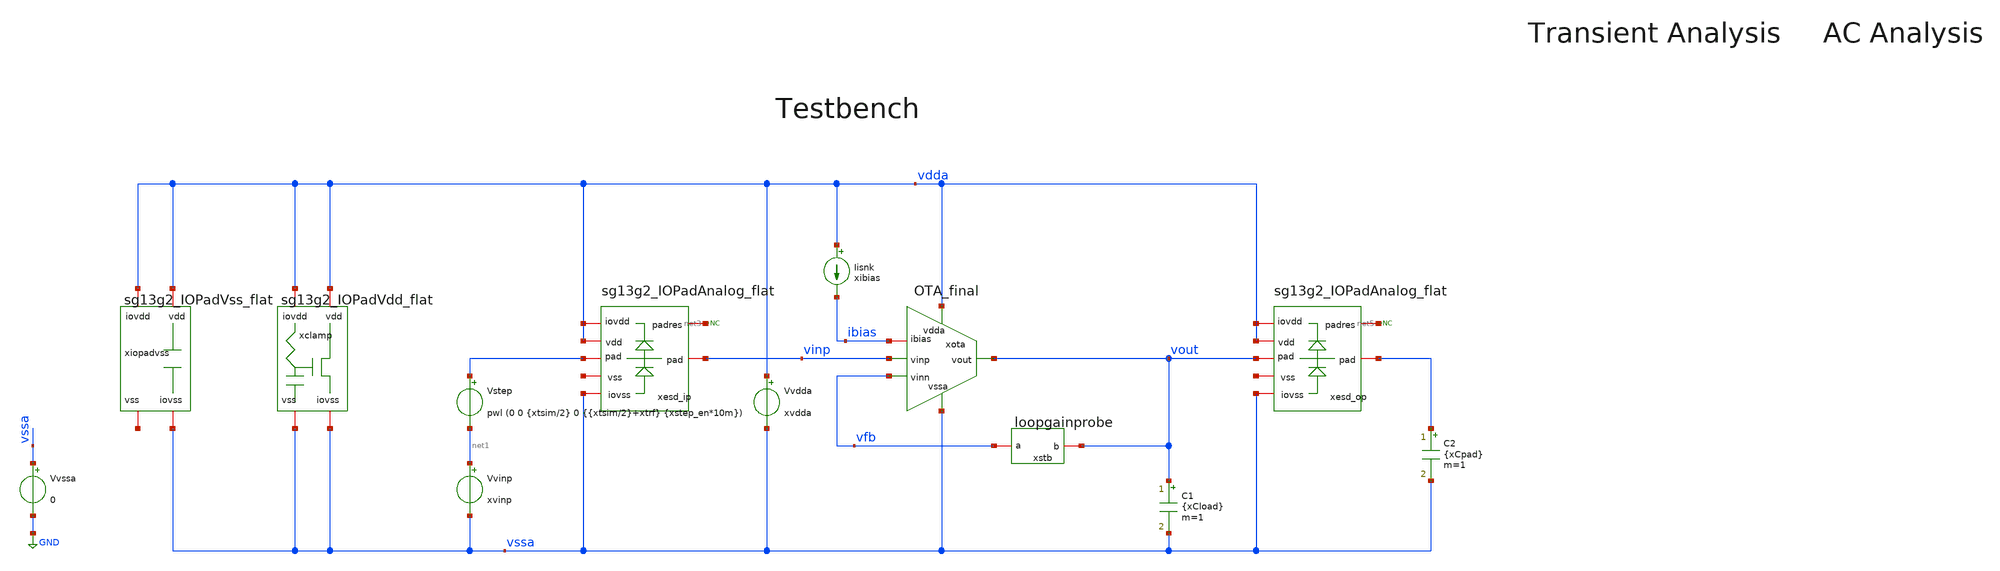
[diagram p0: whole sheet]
** sch_path: tb_OTA_1stage_ihp/tb_OTA_esd_analysis.sch
**.subckt tb_OTA_esd_analysis
Vvdda vdda vssa xvdda
Iisnk vdda ibias xibias
xota vdda vinp vfb vssa vout ibias OTA_final
Vstep vinp net1 pwl (0 0 {xtsim/2} 0 {{xtsim/2}+xtrf} {xstep_en*10m})
Vvinp net1 vssa xvinp
Vvssa vssa GND 0
xstb vfb vout loopgainprobe
xclamp vdda vssa vdda vssa sg13g2_IOPadVdd_flat
xiopadvss vdda vssa vdda net2 sg13g2_IOPadVss_flat
* noconn #net3
xesd_ip vdda vssa net3 vdda vinp net4 sg13g2_IOPadAnalog_flat
C1 vout vssa {xCload} m=1
xesd_op vdda vssa net5 vdda vout net6 sg13g2_IOPadAnalog_flat
C2 vout vssa {xCpad} m=1
* noconn #net5
**** begin user architecture code

** opencircuitdesign pdks install
.lib /home/slice/pdk/iHP/IHP-Open-PDK/ihp-sg13g2/libs.tech/ngspice/models/cornerMOSlv.lib mos_tt
*.lib /home/slice/pdk/iHP/IHP-Open-PDK/ihp-sg13g2/libs.tech/ngspice/models/sg13g2_moshv_mod.lib
.lib /home/slice/pdk/iHP/IHP-Open-PDK/ihp-sg13g2/libs.tech/ngspice/models/cornerMOShv.lib mos_tt
.lib /home/slice/pdk/iHP/IHP-Open-PDK/ihp-sg13g2/libs.tech/ngspice/models/cornerRES.lib res_typ
.include /home/slice/pdk/iHP/IHP-Open-PDK/ihp-sg13g2/libs.tech/ngspice/models/diodes.lib
*.lib /home/slice/xschem/tb_OTA_1stage_ihp/cornerRES.lib res_typ
*.lib /home/slice/xschem/tb_OTA_1stage_ihp/resistors_mod.lib

*.model
*+ /home/slice/pdk/iHP/IHP-Open-PDK/ihp-sg13g2/libs.tech/ngspice/models/sg13g2_moshv_mod.lib/sg13_hv_pmos

*.model /home/slice/Desktop/acm2/MOSFET_model/Verilog-A/NMOS_ACM_2V0.va
*.model /home/slice/Desktop/acm2/MOSFET_model/Verilog-A/PMOS_ACM_2V0.va

* Parameters
.param xvdda = 1.8
.param xvinp = 1
.param xibias = 40u
.param xCload = 0p
.param xCpad = 100f
.param xgm_dp = 1e-3
.param xRin = 1/xgm_dp
.param xCout = 1p
.param xRout = 1e6
.param xtrf = 50p
.param xtsim = 5u
.param xstep_en = 1

* vlogA instantiation
.model OTA_vcvs OTA_vcvs


  ** must save the below for DCOP analysis to be back annotated onto the schematic
  .option savecurrents

  .include tb_OTA.save
  .save v(vout) v(vinp) v(vfb) v(vdda) v(xota.pdio) v(xota.vtail) v(vout_pad)
  .save i(v.xota.Virhs) i(v.xota.Vitail) i(xota.vdda) i(v.Vdda)
  .save i(@n.xota.xm6.nsg13_lv_pmos[ids])


  .control
  let xtsim = 0.1u
  pre_osdi OTA_vcvs.osdi
  save all

** 1. DCOP ANALYSIS **

  op
 * set filetype=ascii
  remzerovec
  write tb_OTA_op.raw

** 2. TRAN ANALYSIS **

  tran 1n $&xtsim
  *set filetype=ascii
  remzerovec
  write tb_OTA_tran.raw

** 3. AC ANALYSIS **

  alter i.xstb.Ii acmag=0
  alter v.xstb.Vi acmag=1

  ac dec 10 1 100G

  remzerovec
  write tb_OTA_1stage_ac1.raw

  alter i.xstb.Ii acmag=1
  alter v.xstb.Vi acmag=0

  ac dec 10 1 100G

  * use this line if you want the phase response to start at 180deg
  *let av = {1/(1-1/(2*(ac1.i(v.xstb.Vi)*ac2.v(xstb.x)-ac1.v(xstb.x)*ac2.i(v.xstb.Vi))+ac1.v(xstb.x)+ac2.i(v.xstb.Vi)))}

  * use this line if you want the phase response to start at 0deg (more conventional and directly
+ corresponds to Franks derivation)
  let av = {1/(1/(2*(ac1.i(v.xstb.Vi)*ac2.v(xstb.x)-ac1.v(xstb.x)*ac2.i(v.xstb.Vi))+ac1.v(xstb.x)+ac2.i(v.xstb.Vi))-1)}

  remzerovec
  write tb_OTA_1stage_ac2.raw

  ** 4. MEASURES **

  let n45_rads = -45*(pi/180)
  meas AC Av_0 FIND vdb(av) AT=10
  echo --
  meas AC BW WHEN vp(av)=n45_rads CROSS=1
  echo --
  meas AC Av_BW FIND vdb(av) WHEN vp(av)=n45_rads CROSS=1
  echo --
  meas AC ULGF WHEN vdb(av)=0
  echo --
  meas AC ULGF_phi_rads FIND vp(av) WHEN vdb(av)=0 CROSS=1
  let ULGF_phi_deg = ULGF_phi_rads*(180/pi)
  print ULGF_phi_deg
  let PM = 180+ULGF_phi_deg
  print PM
  echo --
  * putting in -170 since this is a 2nd-order system so doesnt ever achieve -180
  let n180_rads = -170*(pi/180)
  meas AC GM FIND vdb(av) WHEN vp(av)=n180_rads CROSS=1

  setplot
*quit 0
.endc




**** end user architecture code
**.ends

* expanding   symbol:  OTA_final.sym # of pins=6
** sym_path: tb_OTA_1stage_ihp/LAYOUT_demo/OTA.sym
.include /home/slice/xschem/tb_OTA_1stage_ihp/LAYOUT_demo/OTA_final_C.spice

* expanding   symbol:  devices/loopgainprobe.sym # of pins=2
** sym_path: tb_OTA_1stage_ihp/loopgainprobe.sym
** sch_path: tb_OTA_1stage_ihp/loopgainprobe.sch
.subckt loopgainprobe a b
*.iopin b
*.iopin a
**** begin user architecture code
Ii 0 x DC 0 AC 0
Vi x a DC 0 AC 1
Vnodebuffer b x 0
**** end user architecture code
.ends


* expanding   symbol:  sg13g2_IOPadVdd_flat.sym # of pins=4
** sym_path: tb_OTA_1stage_ihp/sg13g2_IOPadVdd.sym
.include /home/slice/xschem/tb_OTA_1stage_ihp/PadRing/sg13g2_IOPadVdd_flat_C.spice

* expanding   symbol:  sg13g2_IOPadVss_flat.sym # of pins=4
** sym_path: tb_OTA_1stage_ihp/sg13g2_IOPadVss.sym
.include /home/slice/xschem/tb_OTA_1stage_ihp/PadRing/sg13g2_IOPadVss_flat_C.spice

* expanding   symbol:  sg13g2_IOPadAnalog_flat.sym # of pins=7
** sym_path: tb_OTA_1stage_ihp/sg13g2_IOPadAnalog.sym
.include /home/slice/xschem/tb_OTA_1stage_ihp/PadRing/sg13g2_IOPadAnalog_flat_C.spice
.GLOBAL GND
.end
